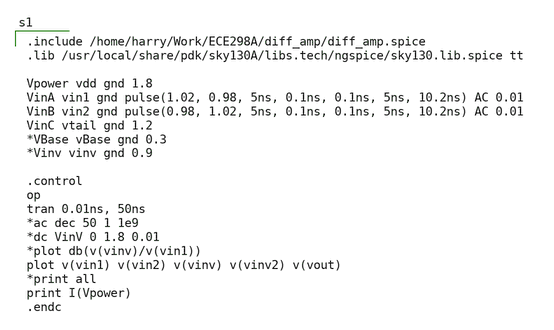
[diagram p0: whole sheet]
** sch_path: magic_xschem_ngspice/Magic_sim.sch
**.subckt Magic_sim
**** begin user architecture code

.include /home/harry/Work/ECE298A/diff_amp/diff_amp.spice
.lib /usr/local/share/pdk/sky130A/libs.tech/ngspice/sky130.lib.spice tt

Vpower vdd gnd 1.8
VinA vin1 gnd pulse(1.02, 0.98, 5ns, 0.1ns, 0.1ns, 5ns, 10.2ns) AC 0.01
VinB vin2 gnd pulse(0.98, 1.02, 5ns, 0.1ns, 0.1ns, 5ns, 10.2ns) AC 0.01
VinC vtail gnd 1.2
*VBase vBase gnd 0.3
*Vinv vinv gnd 0.9

.control
op
tran 0.01ns, 50ns
*ac dec 50 1 1e9
*dc VinV 0 1.8 0.01
*plot db(v(vinv)/v(vin1))
plot v(vin1) v(vin2) v(vinv) v(vinv2) v(vout)
*print all
print I(Vpower)
.endc

**** end user architecture code
**.ends
.end
